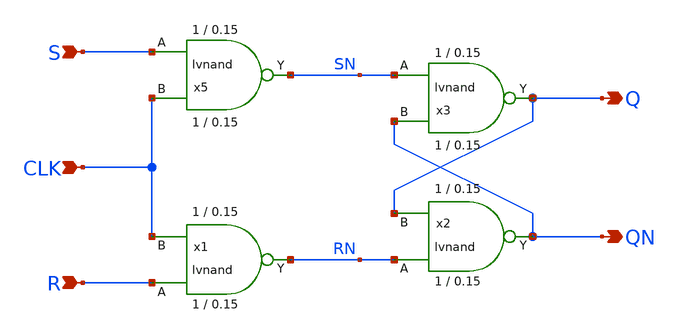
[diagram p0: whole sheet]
** sch_path: sky130_tests/srlatch.sch
* Copyright 2021 Stefan Frederik Schippers
* Licensed under the Apache License, Version 2.0 (the "License");
* you may not use this file except in compliance with the License.
* You may obtain a copy of the License at
* https://www.apache.org/licenses/LICENSE-2.0
* Unless required by applicable law or agreed to in writing, software
* distributed under the License is distributed on an "AS IS" BASIS,
* WITHOUT WARRANTIES OR CONDITIONS OF ANY KIND, either express or implied.
* See the License for the specific language governing permissions and
* limitations under the License.
**.subckt srlatch S R Q QN CLK
*.ipin S
*.ipin R
*.opin Q
*.opin QN
*.ipin CLK
x5 S CLK SN lvnand WidthN=1 LenN=0.15 WidthP=1 LenP=0.15 m=1
x1 R CLK RN lvnand WidthN=1 LenN=0.15 WidthP=1 LenP=0.15 m=1
x2 RN Q QN lvnand WidthN=1 LenN=0.15 WidthP=1 LenP=0.15 m=1
x3 SN QN Q lvnand WidthN=1 LenN=0.15 WidthP=1 LenP=0.15 m=1
**** begin user architecture code

** opencircuitdesign pdks install
.lib $::SKYWATER_MODELS/sky130.lib.spice tt_mm

**** end user architecture code
**.ends

* expanding   symbol:  sky130_tests/lvnand.sym # of pins=3
** sym_path: sky130_tests/lvnand.sym
** sch_path: sky130_tests/lvnand.sch
.subckt lvnand A B Y  WidthN=1 LenN=0.15 WidthP=1 LenP=0.15
*.ipin A
*.ipin B
*.opin Y
XM1 Y B S VSSPIN sky130_fd_pr__nfet_01v8 L=LenN W=WidthN nf=1 ad='int((1 + 1)/2) * WidthN / 1 * 0.29'
+ as='int((1 + 2)/2) * WidthN / 1 * 0.29' pd='2*int((1 + 1)/2) * (WidthN / 1 + 0.29)' ps='2*int((1 + 2)/2) * (WidthN / 1 + 0.29)'
+ nrd='0.29 / WidthN ' nrs='0.29 / WidthN ' sa=0 sb=0 sd=0 mult=1 m=1
XM2 Y A VCCPIN VCCPIN sky130_fd_pr__pfet_01v8 L=LenP W=WidthP nf=1 ad='int((1 + 1)/2) * WidthP / 1 * 0.29'
+ as='int((1 + 2)/2) * WidthP / 1 * 0.29' pd='2*int((1 + 1)/2) * (WidthP / 1 + 0.29)' ps='2*int((1 + 2)/2) * (WidthP / 1 + 0.29)'
+ nrd='0.29 / WidthP ' nrs='0.29 / WidthP ' sa=0 sb=0 sd=0 mult=1 m=1
XM3 Y B VCCPIN VCCPIN sky130_fd_pr__pfet_01v8 L=LenP W=WidthP nf=1 ad='int((1 + 1)/2) * WidthP / 1 * 0.29'
+ as='int((1 + 2)/2) * WidthP / 1 * 0.29' pd='2*int((1 + 1)/2) * (WidthP / 1 + 0.29)' ps='2*int((1 + 2)/2) * (WidthP / 1 + 0.29)'
+ nrd='0.29 / WidthP ' nrs='0.29 / WidthP ' sa=0 sb=0 sd=0 mult=1 m=1
XM4 S A VSSPIN VSSPIN sky130_fd_pr__nfet_01v8 L=LenN W=WidthN nf=1 ad='int((1 + 1)/2) * WidthN / 1 * 0.29'
+ as='int((1 + 2)/2) * WidthN / 1 * 0.29' pd='2*int((1 + 1)/2) * (WidthN / 1 + 0.29)' ps='2*int((1 + 2)/2) * (WidthN / 1 + 0.29)'
+ nrd='0.29 / WidthN ' nrs='0.29 / WidthN ' sa=0 sb=0 sd=0 mult=1 m=1
.ends

**** begin user architecture code

* .option SCALE=1e-6
.option method=gear seed=12
.param L=0.15
.param W=0.5
vd d 0 0
vg g 0 0
.control
dc vd 0 2 0.01 vg 0 2 0.2
alterparam L=0.18
alterparam W=1
reset
dc vd 0 2 0.01 vg 0 2 0.2
alterparam L=0.3
alterparam W=2
reset
dc vd 0 2 0.01 vg 0 2 0.2
alterparam L=0.5
alterparam W=3
reset
dc vd 0 2 0.01 vg 0 2 0.2
.endc


**** end user architecture code
.end
